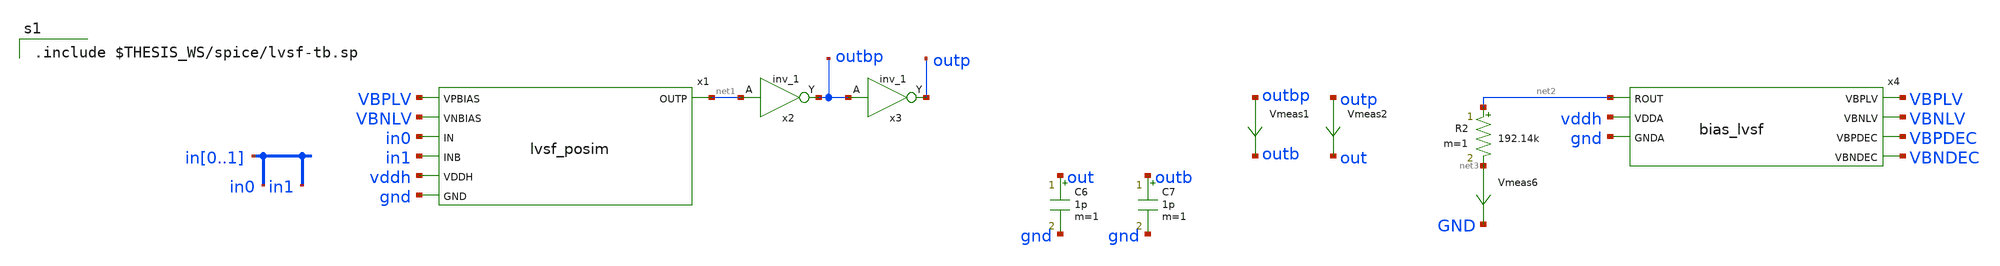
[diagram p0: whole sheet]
** sch_path: xschem/lvsf-tb.sch
.lib $::SKYWATER_MODELS/sky130.lib.spice sf
.include ~/pdk/sky130A/libs.ref/sky130_fd_sc_hvl/spice/sky130_fd_sc_hvl.spice

**.subckt lvsf-tb
C6 out gnd 1p m=1
C7 outb gnd 1p m=1
Vmeas1 outbp outb 0
.save i(vmeas1)
Vmeas2 outp out 0
.save i(vmeas2)
R2 net2 net3 192.14k m=1
Vmeas6 net3 GND 0
.save i(vmeas6)
x4 net2 VBPLV VBNLV VBPDEC VBNDEC vddh gnd bias_lvsf
x1 VBPLV VBNLV in0 in1 net1 vddh gnd lvsf_posim
x2 net1 GND GND VDDH VDDH outbp sky130_fd_sc_hvl__inv_1
x3 outbp GND GND VDDH VDDH outp sky130_fd_sc_hvl__inv_1
**** begin user architecture code

.include $THESIS_WS/spice/lvsf-tb.sp

**** end user architecture code
**.ends

* expanding   symbol:  bias_lvsf.sym # of pins=7
** sym_path: xschem/bias_lvsf.sym
** sch_path: xschem/bias_lvsf.sch
.subckt bias_lvsf ROUT VBPLV VBNLV VBPDEC VBNDEC VDDA GNDA
*.ipin ROUT
*.opin VBPLV
*.opin VBNLV
*.opin VBPDEC
*.opin VBNDEC
*.ipin VDDA
*.ipin GNDA
.param wp_iref=1.8 wn_iref=0.6 miref=2 lref=1 lr=20
XM1 n1 n1 VDDA VDDA sky130_fd_pr__pfet_g5v0d10v5 L=1 W=1.8 nf=1 ad='int((nf+1)/2) * W/nf * 0.29' as='int((nf+2)/2) * W/nf * 0.29'
+ pd='2*int((nf+1)/2) * (W/nf + 0.29)' ps='2*int((nf+2)/2) * (W/nf + 0.29)' nrd='0.29 / W' nrs='0.29 / W'
+ sa=0 sb=0 sd=0 mult=2 m=2
XM2 n2 n2 n1 VDDA sky130_fd_pr__pfet_g5v0d10v5 L=1 W=1.8 nf=1 ad='int((nf+1)/2) * W/nf * 0.29' as='int((nf+2)/2) * W/nf * 0.29'
+ pd='2*int((nf+1)/2) * (W/nf + 0.29)' ps='2*int((nf+2)/2) * (W/nf + 0.29)' nrd='0.29 / W' nrs='0.29 / W'
+ sa=0 sb=0 sd=0 mult=2 m=2
XM3 net1 ROUT n2 VDDA sky130_fd_pr__pfet_g5v0d10v5 L=20 W=1.8 nf=1 ad='int((nf+1)/2) * W/nf * 0.29' as='int((nf+2)/2) * W/nf * 0.29'
+ pd='2*int((nf+1)/2) * (W/nf + 0.29)' ps='2*int((nf+2)/2) * (W/nf + 0.29)' nrd='0.29 / W' nrs='0.29 / W'
+ sa=0 sb=0 sd=0 mult=2 m=2
XM4 ROUT ROUT net1 VDDA sky130_fd_pr__pfet_g5v0d10v5 L=20 W=1.8 nf=1 ad='int((nf+1)/2) * W/nf * 0.29'
+ as='int((nf+2)/2) * W/nf * 0.29' pd='2*int((nf+1)/2) * (W/nf + 0.29)' ps='2*int((nf+2)/2) * (W/nf + 0.29)'
+ nrd='0.29 / W' nrs='0.29 / W' sa=0 sb=0 sd=0 mult=2 m=2
XM5 net2 n1 VDDA VDDA sky130_fd_pr__pfet_g5v0d10v5 L=1 W=1.8 nf=1 ad='int((nf+1)/2) * W/nf * 0.29' as='int((nf+2)/2) * W/nf * 0.29'
+ pd='2*int((nf+1)/2) * (W/nf + 0.29)' ps='2*int((nf+2)/2) * (W/nf + 0.29)' nrd='0.29 / W' nrs='0.29 / W'
+ sa=0 sb=0 sd=0 mult=2 m=2
XM6 n3 n2 net2 VDDA sky130_fd_pr__pfet_g5v0d10v5 L=1 W=1.8 nf=1 ad='int((nf+1)/2) * W/nf * 0.29' as='int((nf+2)/2) * W/nf * 0.29'
+ pd='2*int((nf+1)/2) * (W/nf + 0.29)' ps='2*int((nf+2)/2) * (W/nf + 0.29)' nrd='0.29 / W' nrs='0.29 / W'
+ sa=0 sb=0 sd=0 mult=2 m=2
XM9 net3 n1 VDDA VDDA sky130_fd_pr__pfet_g5v0d10v5 L=1 W=1.8 nf=1 ad='int((nf+1)/2) * W/nf * 0.29' as='int((nf+2)/2) * W/nf * 0.29'
+ pd='2*int((nf+1)/2) * (W/nf + 0.29)' ps='2*int((nf+2)/2) * (W/nf + 0.29)' nrd='0.29 / W' nrs='0.29 / W'
+ sa=0 sb=0 sd=0 mult=2 m=2
XM10 VBNLV n2 net3 VDDA sky130_fd_pr__pfet_g5v0d10v5 L=1 W=1.8 nf=1 ad='int((nf+1)/2) * W/nf * 0.29'
+ as='int((nf+2)/2) * W/nf * 0.29' pd='2*int((nf+1)/2) * (W/nf + 0.29)' ps='2*int((nf+2)/2) * (W/nf + 0.29)'
+ nrd='0.29 / W' nrs='0.29 / W' sa=0 sb=0 sd=0 mult=2 m=2
XM11 net4 n1 VDDA VDDA sky130_fd_pr__pfet_g5v0d10v5 L=1 W=1.8 nf=1 ad='int((nf+1)/2) * W/nf * 0.29' as='int((nf+2)/2) * W/nf * 0.29'
+ pd='2*int((nf+1)/2) * (W/nf + 0.29)' ps='2*int((nf+2)/2) * (W/nf + 0.29)' nrd='0.29 / W' nrs='0.29 / W'
+ sa=0 sb=0 sd=0 mult=2 m=2
XM12 VBNDEC n2 net4 VDDA sky130_fd_pr__pfet_g5v0d10v5 L=1 W=1.8 nf=1 ad='int((nf+1)/2) * W/nf * 0.29'
+ as='int((nf+2)/2) * W/nf * 0.29' pd='2*int((nf+1)/2) * (W/nf + 0.29)' ps='2*int((nf+2)/2) * (W/nf + 0.29)'
+ nrd='0.29 / W' nrs='0.29 / W' sa=0 sb=0 sd=0 mult=2 m=2
XM22 net6 n1 VDDA VDDA sky130_fd_pr__pfet_g5v0d10v5 L=1 W=1.8 nf=1 ad='int((nf+1)/2) * W/nf * 0.29' as='int((nf+2)/2) * W/nf * 0.29'
+ pd='2*int((nf+1)/2) * (W/nf + 0.29)' ps='2*int((nf+2)/2) * (W/nf + 0.29)' nrd='0.29 / W' nrs='0.29 / W'
+ sa=0 sb=0 sd=0 mult=2 m=2
XM23 VBPDEC n2 net6 VDDA sky130_fd_pr__pfet_g5v0d10v5 L=1 W=1.8 nf=1 ad='int((nf+1)/2) * W/nf * 0.29'
+ as='int((nf+2)/2) * W/nf * 0.29' pd='2*int((nf+1)/2) * (W/nf + 0.29)' ps='2*int((nf+2)/2) * (W/nf + 0.29)'
+ nrd='0.29 / W' nrs='0.29 / W' sa=0 sb=0 sd=0 mult=2 m=2
XM7 n3 n3 n4 GNDA sky130_fd_pr__nfet_g5v0d10v5 L=1 W=0.6 nf=1 ad='int((nf+1)/2) * W/nf * 0.29' as='int((nf+2)/2) * W/nf * 0.29'
+ pd='2*int((nf+1)/2) * (W/nf + 0.29)' ps='2*int((nf+2)/2) * (W/nf + 0.29)' nrd='0.29 / W' nrs='0.29 / W'
+ sa=0 sb=0 sd=0 mult=2 m=2
XM8 n4 n4 GNDA GNDA sky130_fd_pr__nfet_g5v0d10v5 L=1 W=0.6 nf=1 ad='int((nf+1)/2) * W/nf * 0.29' as='int((nf+2)/2) * W/nf * 0.29'
+ pd='2*int((nf+1)/2) * (W/nf + 0.29)' ps='2*int((nf+2)/2) * (W/nf + 0.29)' nrd='0.29 / W' nrs='0.29 / W'
+ sa=0 sb=0 sd=0 mult=2 m=2
XM13 VBPLV n3 net5 GNDA sky130_fd_pr__nfet_g5v0d10v5 L=1 W=0.6 nf=1 ad='int((nf+1)/2) * W/nf * 0.29'
+ as='int((nf+2)/2) * W/nf * 0.29' pd='2*int((nf+1)/2) * (W/nf + 0.29)' ps='2*int((nf+2)/2) * (W/nf + 0.29)'
+ nrd='0.29 / W' nrs='0.29 / W' sa=0 sb=0 sd=0 mult=2 m=2
XM15 net5 n4 GNDA GNDA sky130_fd_pr__nfet_g5v0d10v5 L=1 W=0.6 nf=1 ad='int((nf+1)/2) * W/nf * 0.29' as='int((nf+2)/2) * W/nf * 0.29'
+ pd='2*int((nf+1)/2) * (W/nf + 0.29)' ps='2*int((nf+2)/2) * (W/nf + 0.29)' nrd='0.29 / W' nrs='0.29 / W'
+ sa=0 sb=0 sd=0 mult=2 m=2
XM19 VBNLV VBNLV n6 GNDA sky130_fd_pr__nfet_g5v0d10v5 L=1 W=0.6 nf=1 ad='int((nf+1)/2) * W/nf * 0.29'
+ as='int((nf+2)/2) * W/nf * 0.29' pd='2*int((nf+1)/2) * (W/nf + 0.29)' ps='2*int((nf+2)/2) * (W/nf + 0.29)'
+ nrd='0.29 / W' nrs='0.29 / W' sa=0 sb=0 sd=0 mult=2 m=2
XM20 VBNDEC VBNDEC n7 GNDA sky130_fd_pr__nfet_g5v0d10v5 L=1 W=0.6 nf=1 ad='int((nf+1)/2) * W/nf * 0.29'
+ as='int((nf+2)/2) * W/nf * 0.29' pd='2*int((nf+1)/2) * (W/nf + 0.29)' ps='2*int((nf+2)/2) * (W/nf + 0.29)'
+ nrd='0.29 / W' nrs='0.29 / W' sa=0 sb=0 sd=0 mult=2 m=2
XM25 VBPDEC VBPDEC n14 GNDA sky130_fd_pr__nfet_g5v0d10v5 L=1 W=0.6 nf=1 ad='int((nf+1)/2) * W/nf * 0.29'
+ as='int((nf+2)/2) * W/nf * 0.29' pd='2*int((nf+1)/2) * (W/nf + 0.29)' ps='2*int((nf+2)/2) * (W/nf + 0.29)'
+ nrd='0.29 / W' nrs='0.29 / W' sa=0 sb=0 sd=0 mult=2 m=2
XM14 n6 VBNLV GNDA GNDA sky130_fd_pr__nfet_g5v0d10v5 L=5.3 W=0.6 nf=1 ad='int((nf+1)/2) * W/nf * 0.29'
+ as='int((nf+2)/2) * W/nf * 0.29' pd='2*int((nf+1)/2) * (W/nf + 0.29)' ps='2*int((nf+2)/2) * (W/nf + 0.29)'
+ nrd='0.29 / W' nrs='0.29 / W' sa=0 sb=0 sd=0 mult=1 m=1
XM16 n7 VBNDEC GNDA GNDA sky130_fd_pr__nfet_g5v0d10v5 L=9.7 W=0.61 nf=1 ad='int((nf+1)/2) * W/nf * 0.29'
+ as='int((nf+2)/2) * W/nf * 0.29' pd='2*int((nf+1)/2) * (W/nf + 0.29)' ps='2*int((nf+2)/2) * (W/nf + 0.29)'
+ nrd='0.29 / W' nrs='0.29 / W' sa=0 sb=0 sd=0 mult=1 m=1
XM27 n14 n14 GNDA GNDA sky130_fd_pr__nfet_g5v0d10v5 L=12 W=0.64 nf=1 ad='int((nf+1)/2) * W/nf * 0.29'
+ as='int((nf+2)/2) * W/nf * 0.29' pd='2*int((nf+1)/2) * (W/nf + 0.29)' ps='2*int((nf+2)/2) * (W/nf + 0.29)'
+ nrd='0.29 / W' nrs='0.29 / W' sa=0 sb=0 sd=0 mult=1 m=1
XM18 VBPLV VBPLV n10 VDDA sky130_fd_pr__pfet_g5v0d10v5 L=1 W=1.8 nf=1 ad='int((nf+1)/2) * W/nf * 0.29'
+ as='int((nf+2)/2) * W/nf * 0.29' pd='2*int((nf+1)/2) * (W/nf + 0.29)' ps='2*int((nf+2)/2) * (W/nf + 0.29)'
+ nrd='0.29 / W' nrs='0.29 / W' sa=0 sb=0 sd=0 mult=2 m=2
XM17 n10 VBPLV VDDA VDDA sky130_fd_pr__pfet_g5v0d10v5 L=9.2 W=1 nf=1 ad='int((nf+1)/2) * W/nf * 0.29'
+ as='int((nf+2)/2) * W/nf * 0.29' pd='2*int((nf+1)/2) * (W/nf + 0.29)' ps='2*int((nf+2)/2) * (W/nf + 0.29)'
+ nrd='0.29 / W' nrs='0.29 / W' sa=0 sb=0 sd=0 mult=1 m=1
XM28 VDDA VDDA VDDA VDDA sky130_fd_pr__pfet_g5v0d10v5 L=20 W=1.8 nf=1 ad='int((nf+1)/2) * W/nf * 0.29'
+ as='int((nf+2)/2) * W/nf * 0.29' pd='2*int((nf+1)/2) * (W/nf + 0.29)' ps='2*int((nf+2)/2) * (W/nf + 0.29)'
+ nrd='0.29 / W' nrs='0.29 / W' sa=0 sb=0 sd=0 mult=2 m=2
XM29 VDDA VDDA VDDA VDDA sky130_fd_pr__pfet_g5v0d10v5 L=20 W=1.8 nf=1 ad='int((nf+1)/2) * W/nf * 0.29'
+ as='int((nf+2)/2) * W/nf * 0.29' pd='2*int((nf+1)/2) * (W/nf + 0.29)' ps='2*int((nf+2)/2) * (W/nf + 0.29)'
+ nrd='0.29 / W' nrs='0.29 / W' sa=0 sb=0 sd=0 mult=2 m=2
.ends

.end
